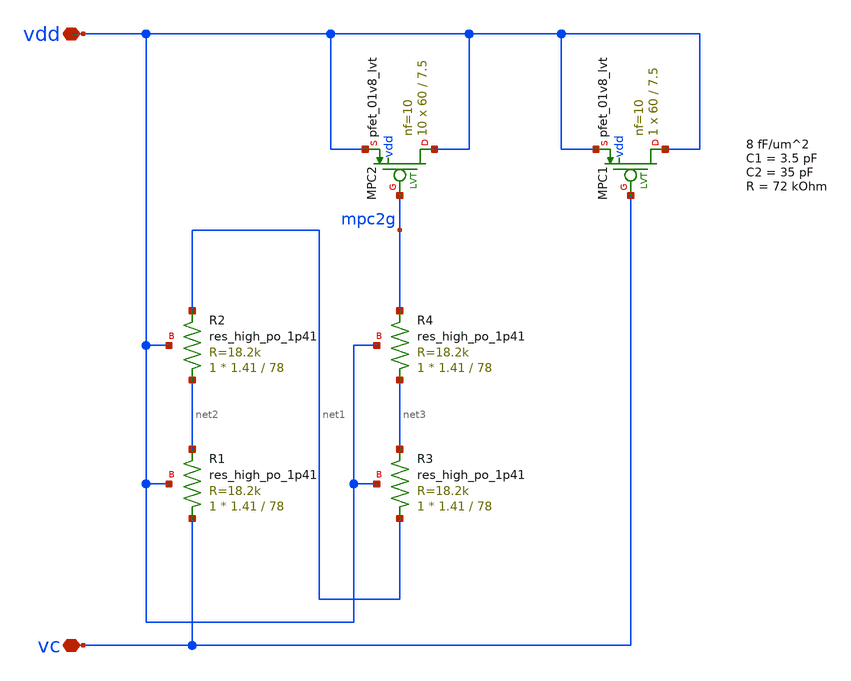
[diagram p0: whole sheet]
** sch_path: xschem/ejf_pll96_lpf.sch
**.subckt ejf_pll96_lpf vc vdd
*.iopin vc
*.iopin vdd
XMPC2 vdd mpc2g vdd vdd sky130_fd_pr__pfet_01v8_lvt L=7.5 W=60 nf=10 ad='int((nf+1)/2) * W/nf * 0.29'
+ as='int((nf+2)/2) * W/nf * 0.29' pd='2*int((nf+1)/2) * (W/nf + 0.29)' ps='2*int((nf+2)/2) * (W/nf + 0.29)'
+ nrd='0.29 / W' nrs='0.29 / W' sa=0 sb=0 sd=0 mult=10 m=10
XMPC1 vdd vc vdd vdd sky130_fd_pr__pfet_01v8_lvt L=7.5 W=60 nf=10 ad='int((nf+1)/2) * W/nf * 0.29' as='int((nf+2)/2) * W/nf * 0.29'
+ pd='2*int((nf+1)/2) * (W/nf + 0.29)' ps='2*int((nf+2)/2) * (W/nf + 0.29)' nrd='0.29 / W' nrs='0.29 / W'
+ sa=0 sb=0 sd=0 mult=1 m=1
XR1 vc net2 vdd sky130_fd_pr__res_high_po_1p41 L=78 mult=1 m=1
XR2 net2 net1 vdd sky130_fd_pr__res_high_po_1p41 L=78 mult=1 m=1
XR3 net1 net3 vdd sky130_fd_pr__res_high_po_1p41 L=78 mult=1 m=1
XR4 net3 mpc2g vdd sky130_fd_pr__res_high_po_1p41 L=78 mult=1 m=1
**.ends
.end
